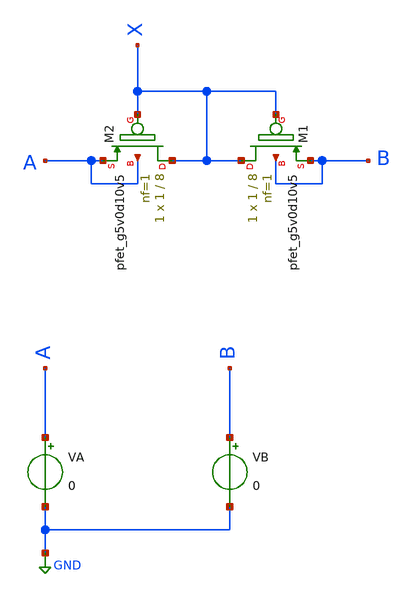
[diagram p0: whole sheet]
** sch_path: xschem/MISC/pseudo/pseudo_tb.sch
* Copyright 2020 Stefan Frederik Schippers
* Licensed under the Apache License, Version 2.0 (the "License");
* you may not use this file except in compliance with the License.
* You may obtain a copy of the License at
* https://www.apache.org/licenses/LICENSE-2.0
* Unless required by applicable law or agreed to in writing, software
* distributed under the License is distributed on an "AS IS" BASIS,
* WITHOUT WARRANTIES OR CONDITIONS OF ANY KIND, either express or implied.
* See the License for the specific language governing permissions and
* limitations under the License.
**.subckt pseudo_tb
XM1 X X B B sky130_fd_pr__pfet_g5v0d10v5 L=8 W=1 nf=1 ad='int((nf+1)/2) * W/nf * 0.29' as='int((nf+2)/2) * W/nf * 0.29'
+ pd='2*int((nf+1)/2) * (W/nf + 0.29)' ps='2*int((nf+2)/2) * (W/nf + 0.29)' nrd='0.29 / W' nrs='0.29 / W'
+ sa=0 sb=0 sd=0 mult=1 m=1
XM2 X X A A sky130_fd_pr__pfet_g5v0d10v5 L=8 W=1 nf=1 ad='int((nf+1)/2) * W/nf * 0.29' as='int((nf+2)/2) * W/nf * 0.29'
+ pd='2*int((nf+1)/2) * (W/nf + 0.29)' ps='2*int((nf+2)/2) * (W/nf + 0.29)' nrd='0.29 / W' nrs='0.29 / W'
+ sa=0 sb=0 sd=0 mult=1 m=1
VA A GND 0
VB B GND 0
**** begin user architecture code


.include ~/git/open_pdks/sources/sky130-pdk/libraries/sky130_fd_pr/latest/cells/pfet_g5v0d10v5/sky130_fd_pr__pfet_g5v0d10v5__tt.corner.spice
.include ~/git/open_pdks/sources/sky130-pdk/libraries/sky130_fd_pr/latest/cells/pfet_g5v0d10v5/sky130_fd_pr__pfet_g5v0d10v5__mismatch.corner.spice
.include ~/git/open_pdks/sources/sky130-pdk/libraries/sky130_fd_pr/latest/models/all.spice

* All models
*.include /usr/share/pdk/sky130A/libs.tech/ngspice/sky130.lib.spice




.options gmin=1e-13
.options rshunt = 1.0e13

.control
  dc VA -0.9 0.9 0.011
  let r=abs(deriv(v(a))/deriv(i(va)))
  plot r ylog
.endc


**** end user architecture code
**.ends
.GLOBAL GND
.end
